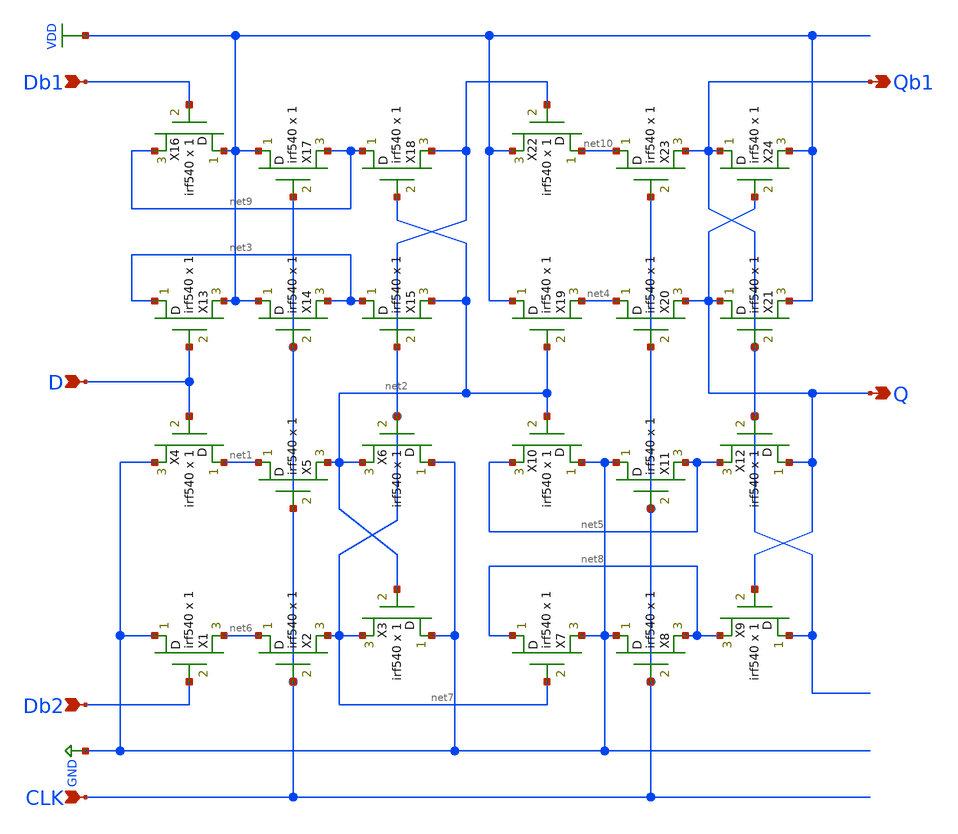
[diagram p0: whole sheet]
** sch_path: projects/negdff/xschem_ngspice/negdff.sch
**.subckt negdff D Db1 Db2 Q Qb1 CLK
*.ipin D
*.ipin Db1
*.ipin Db2
*.opin Q
*.opin Qb1
*.ipin CLK
X1 GND Db2 net6 irf540 m=1
X2 net6 CLK net7 irf540 m=1
X3 GND net2 net7 irf540 m=1
X4 net1 D GND irf540 m=1
X5 net1 CLK net2 irf540 m=1
X6 GND net7 net2 irf540 m=1
X7 net8 net7 GND irf540 m=1
X8 GND CLK net8 irf540 m=1
X9 Qb1 Q net8 irf540 m=1
X10 GND net2 net5 irf540 m=1
X11 GND CLK net5 irf540 m=1
X12 Q Qb1 net5 irf540 m=1
X13 net3 D VDD irf540 m=1
X14 VDD CLK net3 irf540 m=1
X15 net3 net7 net2 irf540 m=1
X16 VDD Db1 net9 irf540 m=1
X17 VDD CLK net9 irf540 m=1
X18 net9 net2 net7 irf540 m=1
X19 VDD net2 net4 irf540 m=1
X20 net4 CLK Q irf540 m=1
X21 Q Qb1 VDD irf540 m=1
X22 net10 net7 VDD irf540 m=1
X23 net10 CLK Qb1 irf540 m=1
X24 Qb1 Q VDD irf540 m=1
**.ends
.GLOBAL GND
.GLOBAL VDD
.end
